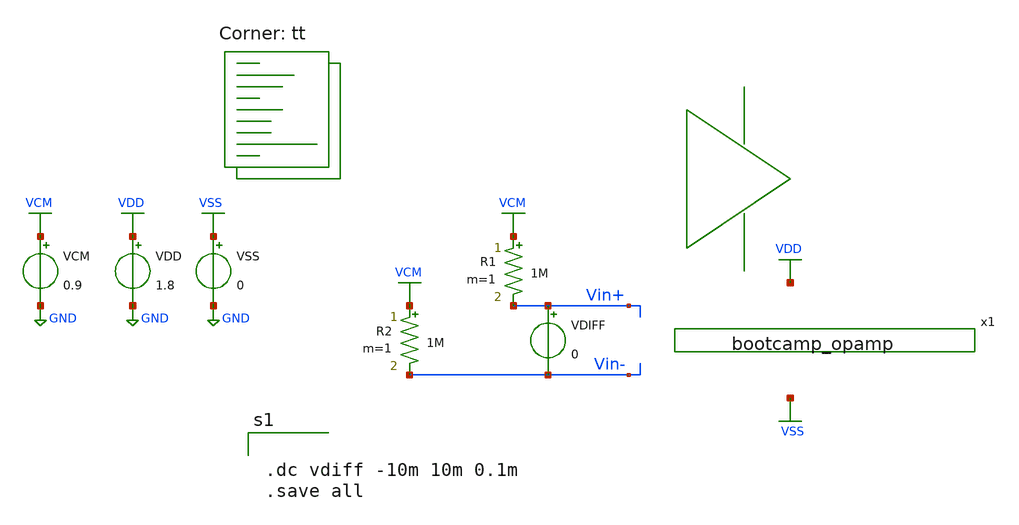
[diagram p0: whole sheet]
** sch_path: analog/schematics/tb_dc_analysis.sch
**.subckt tb_dc_analysis
R1 VCM Vin+ 1M m=1
R2 VCM Vin- 1M m=1
VDD VDD GND 1.8
VCM VCM GND 0.9
VDIFF Vin+ Vin- 0
VSS VSS GND 0
x1 bootcamp_opamp
**** begin user architecture code


.dc vdiff -10m 10m 0.1m
.save all


.lib $::SKYWATER_MODELS/sky130.lib.spice tt
**** end user architecture code
**.ends

* expanding   symbol:  bootcamp_opamp.sym # of pins=0
** sym_path: analog/schematics/bootcamp_opamp.sym
** sch_path: analog/schematics/bootcamp_opamp.sch
.subckt bootcamp_opamp
XM1 net1 net5 net3 net6 sky130_fd_pr__nfet_01v8 L=0.15 W=1 nf=1 ad='int((nf+1)/2) * W/nf * 0.29' as='int((nf+2)/2) * W/nf * 0.29'
+ pd='2*int((nf+1)/2) * (W/nf + 0.29)' ps='2*int((nf+2)/2) * (W/nf + 0.29)' nrd='0.29 / W' nrs='0.29 / W'
+ sa=0 sb=0 sd=0 mult=1 m=1
XM2 net2 net7 net3 net8 sky130_fd_pr__nfet_01v8 L=0.15 W=1 nf=1 ad='int((nf+1)/2) * W/nf * 0.29' as='int((nf+2)/2) * W/nf * 0.29'
+ pd='2*int((nf+1)/2) * (W/nf + 0.29)' ps='2*int((nf+2)/2) * (W/nf + 0.29)' nrd='0.29 / W' nrs='0.29 / W'
+ sa=0 sb=0 sd=0 mult=1 m=1
XM3 net1 net1 net4 net9 sky130_fd_pr__pfet_01v8 L=0.15 W=1 nf=1 ad='int((nf+1)/2) * W/nf * 0.29' as='int((nf+2)/2) * W/nf * 0.29'
+ pd='2*int((nf+1)/2) * (W/nf + 0.29)' ps='2*int((nf+2)/2) * (W/nf + 0.29)' nrd='0.29 / W' nrs='0.29 / W'
+ sa=0 sb=0 sd=0 mult=1 m=1
XM4 net2 net1 net4 net10 sky130_fd_pr__pfet_01v8 L=0.15 W=1 nf=1 ad='int((nf+1)/2) * W/nf * 0.29' as='int((nf+2)/2) * W/nf * 0.29'
+ pd='2*int((nf+1)/2) * (W/nf + 0.29)' ps='2*int((nf+2)/2) * (W/nf + 0.29)' nrd='0.29 / W' nrs='0.29 / W'
+ sa=0 sb=0 sd=0 mult=1 m=1
XM5 net3 net11 net12 net13 sky130_fd_pr__nfet_01v8 L=0.15 W=1 nf=1 ad='int((nf+1)/2) * W/nf * 0.29' as='int((nf+2)/2) * W/nf * 0.29'
+ pd='2*int((nf+1)/2) * (W/nf + 0.29)' ps='2*int((nf+2)/2) * (W/nf + 0.29)' nrd='0.29 / W' nrs='0.29 / W'
+ sa=0 sb=0 sd=0 mult=1 m=1
.ends

.GLOBAL GND
.GLOBAL VDD
.GLOBAL VCM
.GLOBAL VSS
.end
